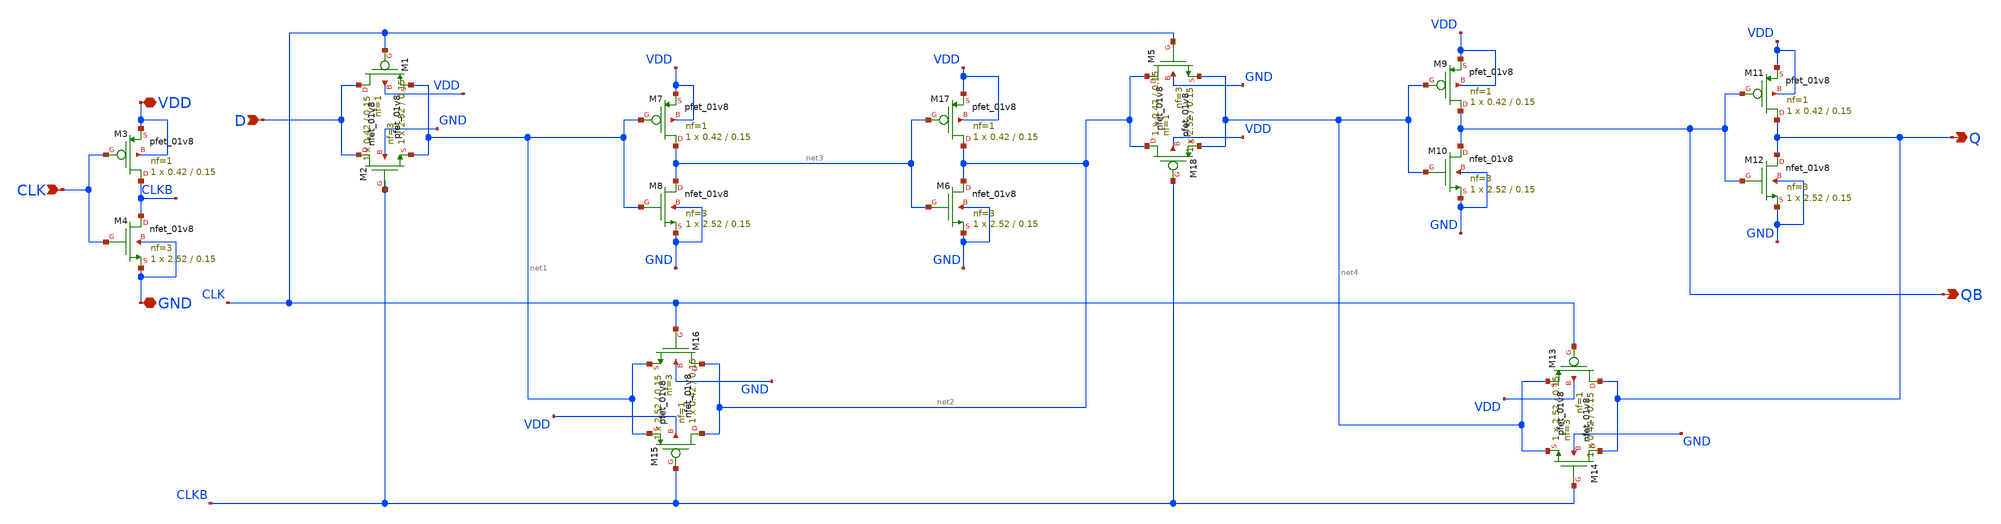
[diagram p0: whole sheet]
** sch_path: cells/DFFX1/schematic/dffx1.sch
**.subckt dffx1 VDD GND CLK D Q QB
*.iopin VDD
*.iopin GND
*.ipin CLK
*.ipin D
*.opin Q
*.opin QB
XM1 D CLK net1 VDD sky130_fd_pr__pfet_01v8 L=0.15 W=0.42 nf=1 ad='int((1 + 1)/2) * 0.42 / 1 * 0.29' as='int((1 + 2)/2) * 0.42 / 1 * 0.29'
+ pd='2*int((1 + 1)/2) * (0.42 / 1 + 0.29)' ps='2*int((1 + 2)/2) * (0.42 / 1 + 0.29)' nrd='0.29 / 0.42 '
+ nrs='0.29 / 0.42 ' sa=0 sb=0 sd=0 mult=1 m=1
XM2 D CLKB net1 GND sky130_fd_pr__nfet_01v8 L=0.15 W=2.52 nf=3 ad='int((3 + 1)/2) * 2.52 / 3 * 0.29'
+ as='int((3 + 2)/2) * 2.52 / 3 * 0.29' pd='2*int((3 + 1)/2) * (2.52 / 3 + 0.29)' ps='2*int((3 + 2)/2) * (2.52 / 3 + 0.29)'
+ nrd='0.29 / 2.52 ' nrs='0.29 / 2.52 ' sa=0 sb=0 sd=0 mult=1 m=1
XM3 CLKB CLK VDD VDD sky130_fd_pr__pfet_01v8 L=0.15 W=0.42 nf=1 ad='int((1 + 1)/2) * 0.42 / 1 * 0.29'
+ as='int((1 + 2)/2) * 0.42 / 1 * 0.29' pd='2*int((1 + 1)/2) * (0.42 / 1 + 0.29)' ps='2*int((1 + 2)/2) * (0.42 / 1 + 0.29)'
+ nrd='0.29 / 0.42 ' nrs='0.29 / 0.42 ' sa=0 sb=0 sd=0 mult=1 m=1
XM4 CLKB CLK GND GND sky130_fd_pr__nfet_01v8 L=0.15 W=2.52 nf=3 ad='int((3 + 1)/2) * 2.52 / 3 * 0.29'
+ as='int((3 + 2)/2) * 2.52 / 3 * 0.29' pd='2*int((3 + 1)/2) * (2.52 / 3 + 0.29)' ps='2*int((3 + 2)/2) * (2.52 / 3 + 0.29)'
+ nrd='0.29 / 2.52 ' nrs='0.29 / 2.52 ' sa=0 sb=0 sd=0 mult=1 m=1
XM14 Q CLKB net4 GND sky130_fd_pr__nfet_01v8 L=0.15 W=2.52 nf=3 ad='int((3 + 1)/2) * 2.52 / 3 * 0.29'
+ as='int((3 + 2)/2) * 2.52 / 3 * 0.29' pd='2*int((3 + 1)/2) * (2.52 / 3 + 0.29)' ps='2*int((3 + 2)/2) * (2.52 / 3 + 0.29)'
+ nrd='0.29 / 2.52 ' nrs='0.29 / 2.52 ' sa=0 sb=0 sd=0 mult=1 m=1
XM13 Q CLK net4 VDD sky130_fd_pr__pfet_01v8 L=0.15 W=0.42 nf=1 ad='int((1 + 1)/2) * 0.42 / 1 * 0.29'
+ as='int((1 + 2)/2) * 0.42 / 1 * 0.29' pd='2*int((1 + 1)/2) * (0.42 / 1 + 0.29)' ps='2*int((1 + 2)/2) * (0.42 / 1 + 0.29)'
+ nrd='0.29 / 0.42 ' nrs='0.29 / 0.42 ' sa=0 sb=0 sd=0 mult=1 m=1
XM7 net3 net1 VDD VDD sky130_fd_pr__pfet_01v8 L=0.15 W=0.42 nf=1 ad='int((1 + 1)/2) * 0.42 / 1 * 0.29'
+ as='int((1 + 2)/2) * 0.42 / 1 * 0.29' pd='2*int((1 + 1)/2) * (0.42 / 1 + 0.29)' ps='2*int((1 + 2)/2) * (0.42 / 1 + 0.29)'
+ nrd='0.29 / 0.42 ' nrs='0.29 / 0.42 ' sa=0 sb=0 sd=0 mult=1 m=1
XM8 net3 net1 GND GND sky130_fd_pr__nfet_01v8 L=0.15 W=2.52 nf=3 ad='int((3 + 1)/2) * 2.52 / 3 * 0.29'
+ as='int((3 + 2)/2) * 2.52 / 3 * 0.29' pd='2*int((3 + 1)/2) * (2.52 / 3 + 0.29)' ps='2*int((3 + 2)/2) * (2.52 / 3 + 0.29)'
+ nrd='0.29 / 2.52 ' nrs='0.29 / 2.52 ' sa=0 sb=0 sd=0 mult=1 m=1
XM17 net2 net3 VDD VDD sky130_fd_pr__pfet_01v8 L=0.15 W=0.42 nf=1 ad='int((1 + 1)/2) * 0.42 / 1 * 0.29'
+ as='int((1 + 2)/2) * 0.42 / 1 * 0.29' pd='2*int((1 + 1)/2) * (0.42 / 1 + 0.29)' ps='2*int((1 + 2)/2) * (0.42 / 1 + 0.29)'
+ nrd='0.29 / 0.42 ' nrs='0.29 / 0.42 ' sa=0 sb=0 sd=0 mult=1 m=1
XM6 net2 net3 GND GND sky130_fd_pr__nfet_01v8 L=0.15 W=2.52 nf=3 ad='int((3 + 1)/2) * 2.52 / 3 * 0.29'
+ as='int((3 + 2)/2) * 2.52 / 3 * 0.29' pd='2*int((3 + 1)/2) * (2.52 / 3 + 0.29)' ps='2*int((3 + 2)/2) * (2.52 / 3 + 0.29)'
+ nrd='0.29 / 2.52 ' nrs='0.29 / 2.52 ' sa=0 sb=0 sd=0 mult=1 m=1
XM9 QB net4 VDD VDD sky130_fd_pr__pfet_01v8 L=0.15 W=0.42 nf=1 ad='int((1 + 1)/2) * 0.42 / 1 * 0.29'
+ as='int((1 + 2)/2) * 0.42 / 1 * 0.29' pd='2*int((1 + 1)/2) * (0.42 / 1 + 0.29)' ps='2*int((1 + 2)/2) * (0.42 / 1 + 0.29)'
+ nrd='0.29 / 0.42 ' nrs='0.29 / 0.42 ' sa=0 sb=0 sd=0 mult=1 m=1
XM10 QB net4 GND GND sky130_fd_pr__nfet_01v8 L=0.15 W=2.52 nf=3 ad='int((3 + 1)/2) * 2.52 / 3 * 0.29'
+ as='int((3 + 2)/2) * 2.52 / 3 * 0.29' pd='2*int((3 + 1)/2) * (2.52 / 3 + 0.29)' ps='2*int((3 + 2)/2) * (2.52 / 3 + 0.29)'
+ nrd='0.29 / 2.52 ' nrs='0.29 / 2.52 ' sa=0 sb=0 sd=0 mult=1 m=1
XM11 Q QB VDD VDD sky130_fd_pr__pfet_01v8 L=0.15 W=0.42 nf=1 ad='int((1 + 1)/2) * 0.42 / 1 * 0.29' as='int((1 + 2)/2) * 0.42 / 1 * 0.29'
+ pd='2*int((1 + 1)/2) * (0.42 / 1 + 0.29)' ps='2*int((1 + 2)/2) * (0.42 / 1 + 0.29)' nrd='0.29 / 0.42 '
+ nrs='0.29 / 0.42 ' sa=0 sb=0 sd=0 mult=1 m=1
XM12 Q QB GND GND sky130_fd_pr__nfet_01v8 L=0.15 W=2.52 nf=3 ad='int((3 + 1)/2) * 2.52 / 3 * 0.29' as='int((3 + 2)/2) * 2.52 / 3 * 0.29'
+ pd='2*int((3 + 1)/2) * (2.52 / 3 + 0.29)' ps='2*int((3 + 2)/2) * (2.52 / 3 + 0.29)' nrd='0.29 / 2.52 '
+ nrs='0.29 / 2.52 ' sa=0 sb=0 sd=0 mult=1 m=1
XM5 net2 CLK net4 GND sky130_fd_pr__nfet_01v8 L=0.15 W=2.52 nf=3 ad='int((3 + 1)/2) * 2.52 / 3 * 0.29'
+ as='int((3 + 2)/2) * 2.52 / 3 * 0.29' pd='2*int((3 + 1)/2) * (2.52 / 3 + 0.29)' ps='2*int((3 + 2)/2) * (2.52 / 3 + 0.29)'
+ nrd='0.29 / 2.52 ' nrs='0.29 / 2.52 ' sa=0 sb=0 sd=0 mult=1 m=1
XM18 net2 CLKB net4 VDD sky130_fd_pr__pfet_01v8 L=0.15 W=0.42 nf=1 ad='int((1 + 1)/2) * 0.42 / 1 * 0.29'
+ as='int((1 + 2)/2) * 0.42 / 1 * 0.29' pd='2*int((1 + 1)/2) * (0.42 / 1 + 0.29)' ps='2*int((1 + 2)/2) * (0.42 / 1 + 0.29)'
+ nrd='0.29 / 0.42 ' nrs='0.29 / 0.42 ' sa=0 sb=0 sd=0 mult=1 m=1
XM15 net2 CLKB net1 VDD sky130_fd_pr__pfet_01v8 L=0.15 W=0.42 nf=1 ad='int((1 + 1)/2) * 0.42 / 1 * 0.29'
+ as='int((1 + 2)/2) * 0.42 / 1 * 0.29' pd='2*int((1 + 1)/2) * (0.42 / 1 + 0.29)' ps='2*int((1 + 2)/2) * (0.42 / 1 + 0.29)'
+ nrd='0.29 / 0.42 ' nrs='0.29 / 0.42 ' sa=0 sb=0 sd=0 mult=1 m=1
XM16 net2 CLK net1 GND sky130_fd_pr__nfet_01v8 L=0.15 W=2.52 nf=3 ad='int((3 + 1)/2) * 2.52 / 3 * 0.29'
+ as='int((3 + 2)/2) * 2.52 / 3 * 0.29' pd='2*int((3 + 1)/2) * (2.52 / 3 + 0.29)' ps='2*int((3 + 2)/2) * (2.52 / 3 + 0.29)'
+ nrd='0.29 / 2.52 ' nrs='0.29 / 2.52 ' sa=0 sb=0 sd=0 mult=1 m=1
**.ends
.end
